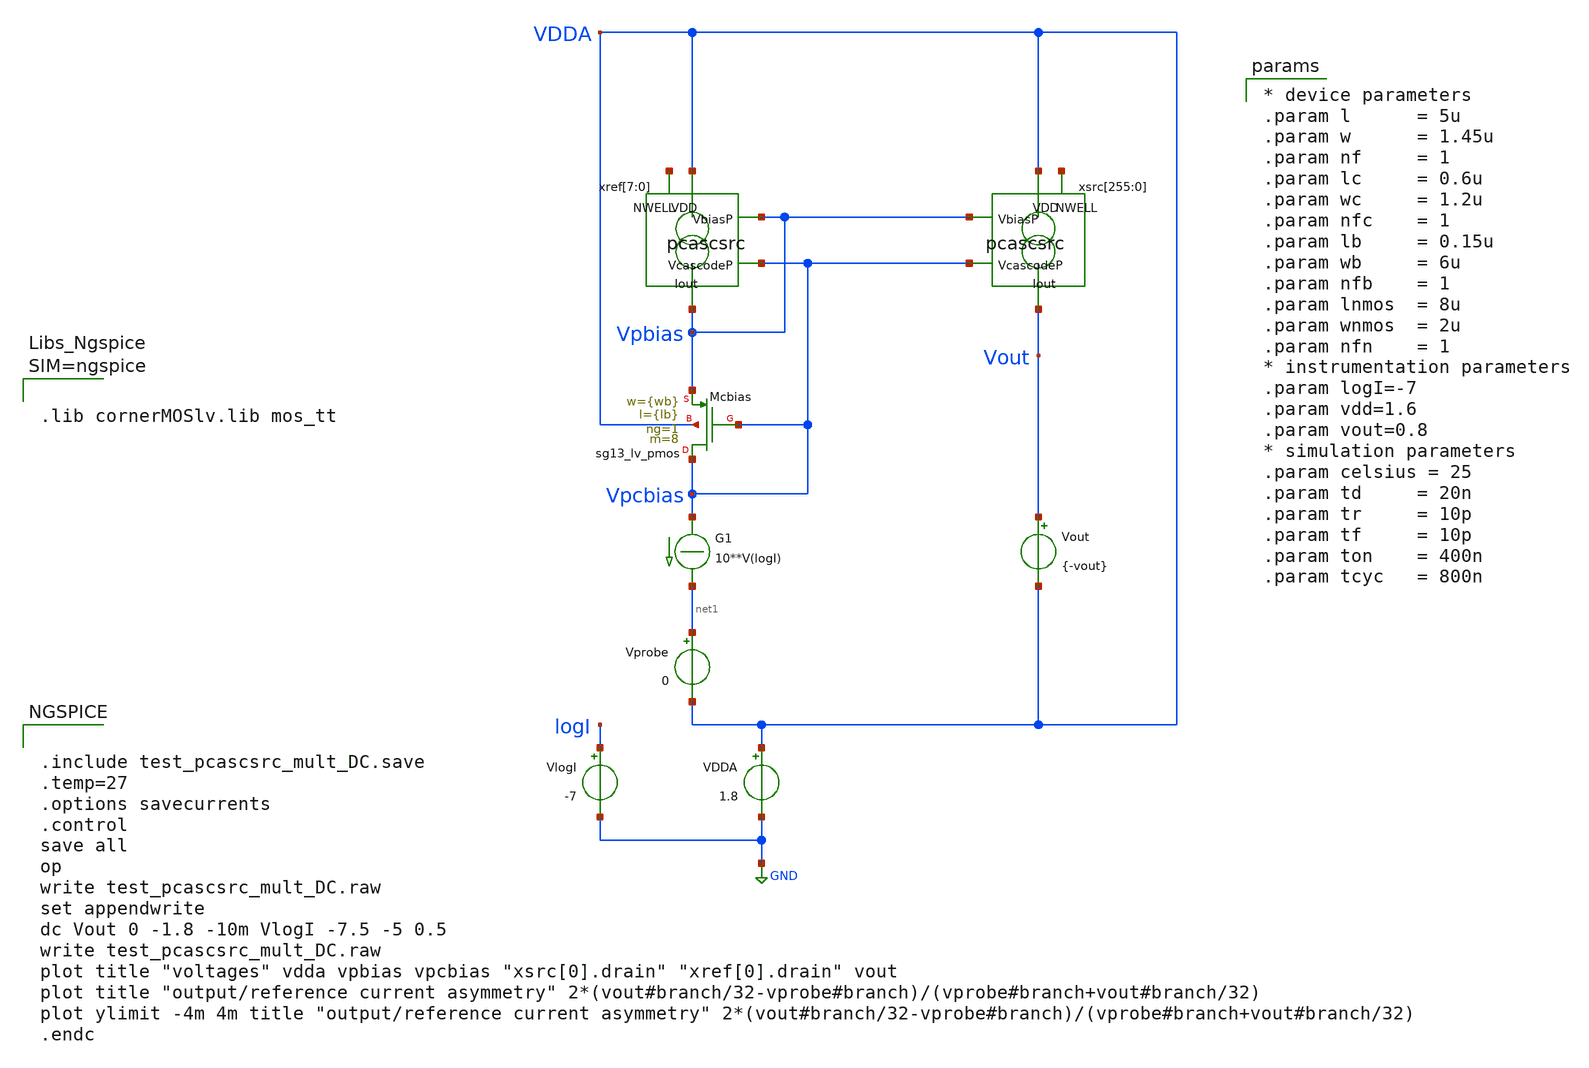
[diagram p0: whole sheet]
** sch_path: xschem/test_pcascsrc_mult_DC.sch
**.subckt test_pcascsrc_mult_DC
Vout Vout VDDA {-vout}
.save i(vout)
Vprobe net1 VDDA 0
.save i(vprobe)
G1 Vpcbias net1 CUR=' 10**V(logI) '
VlogI logI GND -7
.save i(vlogi)
xref[7] VDDA Vpbias Vpcbias Vpbias net2[7] pcascsrc
xref[6] VDDA Vpbias Vpcbias Vpbias net2[6] pcascsrc
xref[5] VDDA Vpbias Vpcbias Vpbias net2[5] pcascsrc
xref[4] VDDA Vpbias Vpcbias Vpbias net2[4] pcascsrc
xref[3] VDDA Vpbias Vpcbias Vpbias net2[3] pcascsrc
xref[2] VDDA Vpbias Vpcbias Vpbias net2[2] pcascsrc
xref[1] VDDA Vpbias Vpcbias Vpbias net2[1] pcascsrc
xref[0] VDDA Vpbias Vpcbias Vpbias net2[0] pcascsrc
xsrc[255] VDDA Vpbias Vpcbias Vout net3[255] pcascsrc
xsrc[254] VDDA Vpbias Vpcbias Vout net3[254] pcascsrc
xsrc[253] VDDA Vpbias Vpcbias Vout net3[253] pcascsrc
xsrc[252] VDDA Vpbias Vpcbias Vout net3[252] pcascsrc
xsrc[251] VDDA Vpbias Vpcbias Vout net3[251] pcascsrc
xsrc[250] VDDA Vpbias Vpcbias Vout net3[250] pcascsrc
xsrc[249] VDDA Vpbias Vpcbias Vout net3[249] pcascsrc
xsrc[248] VDDA Vpbias Vpcbias Vout net3[248] pcascsrc
xsrc[247] VDDA Vpbias Vpcbias Vout net3[247] pcascsrc
xsrc[246] VDDA Vpbias Vpcbias Vout net3[246] pcascsrc
xsrc[245] VDDA Vpbias Vpcbias Vout net3[245] pcascsrc
xsrc[244] VDDA Vpbias Vpcbias Vout net3[244] pcascsrc
xsrc[243] VDDA Vpbias Vpcbias Vout net3[243] pcascsrc
xsrc[242] VDDA Vpbias Vpcbias Vout net3[242] pcascsrc
xsrc[241] VDDA Vpbias Vpcbias Vout net3[241] pcascsrc
xsrc[240] VDDA Vpbias Vpcbias Vout net3[240] pcascsrc
xsrc[239] VDDA Vpbias Vpcbias Vout net3[239] pcascsrc
xsrc[238] VDDA Vpbias Vpcbias Vout net3[238] pcascsrc
xsrc[237] VDDA Vpbias Vpcbias Vout net3[237] pcascsrc
xsrc[236] VDDA Vpbias Vpcbias Vout net3[236] pcascsrc
xsrc[235] VDDA Vpbias Vpcbias Vout net3[235] pcascsrc
xsrc[234] VDDA Vpbias Vpcbias Vout net3[234] pcascsrc
xsrc[233] VDDA Vpbias Vpcbias Vout net3[233] pcascsrc
xsrc[232] VDDA Vpbias Vpcbias Vout net3[232] pcascsrc
xsrc[231] VDDA Vpbias Vpcbias Vout net3[231] pcascsrc
xsrc[230] VDDA Vpbias Vpcbias Vout net3[230] pcascsrc
xsrc[229] VDDA Vpbias Vpcbias Vout net3[229] pcascsrc
xsrc[228] VDDA Vpbias Vpcbias Vout net3[228] pcascsrc
xsrc[227] VDDA Vpbias Vpcbias Vout net3[227] pcascsrc
xsrc[226] VDDA Vpbias Vpcbias Vout net3[226] pcascsrc
xsrc[225] VDDA Vpbias Vpcbias Vout net3[225] pcascsrc
xsrc[224] VDDA Vpbias Vpcbias Vout net3[224] pcascsrc
xsrc[223] VDDA Vpbias Vpcbias Vout net3[223] pcascsrc
xsrc[222] VDDA Vpbias Vpcbias Vout net3[222] pcascsrc
xsrc[221] VDDA Vpbias Vpcbias Vout net3[221] pcascsrc
xsrc[220] VDDA Vpbias Vpcbias Vout net3[220] pcascsrc
xsrc[219] VDDA Vpbias Vpcbias Vout net3[219] pcascsrc
xsrc[218] VDDA Vpbias Vpcbias Vout net3[218] pcascsrc
xsrc[217] VDDA Vpbias Vpcbias Vout net3[217] pcascsrc
xsrc[216] VDDA Vpbias Vpcbias Vout net3[216] pcascsrc
xsrc[215] VDDA Vpbias Vpcbias Vout net3[215] pcascsrc
xsrc[214] VDDA Vpbias Vpcbias Vout net3[214] pcascsrc
xsrc[213] VDDA Vpbias Vpcbias Vout net3[213] pcascsrc
xsrc[212] VDDA Vpbias Vpcbias Vout net3[212] pcascsrc
xsrc[211] VDDA Vpbias Vpcbias Vout net3[211] pcascsrc
xsrc[210] VDDA Vpbias Vpcbias Vout net3[210] pcascsrc
xsrc[209] VDDA Vpbias Vpcbias Vout net3[209] pcascsrc
xsrc[208] VDDA Vpbias Vpcbias Vout net3[208] pcascsrc
xsrc[207] VDDA Vpbias Vpcbias Vout net3[207] pcascsrc
xsrc[206] VDDA Vpbias Vpcbias Vout net3[206] pcascsrc
xsrc[205] VDDA Vpbias Vpcbias Vout net3[205] pcascsrc
xsrc[204] VDDA Vpbias Vpcbias Vout net3[204] pcascsrc
xsrc[203] VDDA Vpbias Vpcbias Vout net3[203] pcascsrc
xsrc[202] VDDA Vpbias Vpcbias Vout net3[202] pcascsrc
xsrc[201] VDDA Vpbias Vpcbias Vout net3[201] pcascsrc
xsrc[200] VDDA Vpbias Vpcbias Vout net3[200] pcascsrc
xsrc[199] VDDA Vpbias Vpcbias Vout net3[199] pcascsrc
xsrc[198] VDDA Vpbias Vpcbias Vout net3[198] pcascsrc
xsrc[197] VDDA Vpbias Vpcbias Vout net3[197] pcascsrc
xsrc[196] VDDA Vpbias Vpcbias Vout net3[196] pcascsrc
xsrc[195] VDDA Vpbias Vpcbias Vout net3[195] pcascsrc
xsrc[194] VDDA Vpbias Vpcbias Vout net3[194] pcascsrc
xsrc[193] VDDA Vpbias Vpcbias Vout net3[193] pcascsrc
xsrc[192] VDDA Vpbias Vpcbias Vout net3[192] pcascsrc
xsrc[191] VDDA Vpbias Vpcbias Vout net3[191] pcascsrc
xsrc[190] VDDA Vpbias Vpcbias Vout net3[190] pcascsrc
xsrc[189] VDDA Vpbias Vpcbias Vout net3[189] pcascsrc
xsrc[188] VDDA Vpbias Vpcbias Vout net3[188] pcascsrc
xsrc[187] VDDA Vpbias Vpcbias Vout net3[187] pcascsrc
xsrc[186] VDDA Vpbias Vpcbias Vout net3[186] pcascsrc
xsrc[185] VDDA Vpbias Vpcbias Vout net3[185] pcascsrc
xsrc[184] VDDA Vpbias Vpcbias Vout net3[184] pcascsrc
xsrc[183] VDDA Vpbias Vpcbias Vout net3[183] pcascsrc
xsrc[182] VDDA Vpbias Vpcbias Vout net3[182] pcascsrc
xsrc[181] VDDA Vpbias Vpcbias Vout net3[181] pcascsrc
xsrc[180] VDDA Vpbias Vpcbias Vout net3[180] pcascsrc
xsrc[179] VDDA Vpbias Vpcbias Vout net3[179] pcascsrc
xsrc[178] VDDA Vpbias Vpcbias Vout net3[178] pcascsrc
xsrc[177] VDDA Vpbias Vpcbias Vout net3[177] pcascsrc
xsrc[176] VDDA Vpbias Vpcbias Vout net3[176] pcascsrc
xsrc[175] VDDA Vpbias Vpcbias Vout net3[175] pcascsrc
xsrc[174] VDDA Vpbias Vpcbias Vout net3[174] pcascsrc
xsrc[173] VDDA Vpbias Vpcbias Vout net3[173] pcascsrc
xsrc[172] VDDA Vpbias Vpcbias Vout net3[172] pcascsrc
xsrc[171] VDDA Vpbias Vpcbias Vout net3[171] pcascsrc
xsrc[170] VDDA Vpbias Vpcbias Vout net3[170] pcascsrc
xsrc[169] VDDA Vpbias Vpcbias Vout net3[169] pcascsrc
xsrc[168] VDDA Vpbias Vpcbias Vout net3[168] pcascsrc
xsrc[167] VDDA Vpbias Vpcbias Vout net3[167] pcascsrc
xsrc[166] VDDA Vpbias Vpcbias Vout net3[166] pcascsrc
xsrc[165] VDDA Vpbias Vpcbias Vout net3[165] pcascsrc
xsrc[164] VDDA Vpbias Vpcbias Vout net3[164] pcascsrc
xsrc[163] VDDA Vpbias Vpcbias Vout net3[163] pcascsrc
xsrc[162] VDDA Vpbias Vpcbias Vout net3[162] pcascsrc
xsrc[161] VDDA Vpbias Vpcbias Vout net3[161] pcascsrc
xsrc[160] VDDA Vpbias Vpcbias Vout net3[160] pcascsrc
xsrc[159] VDDA Vpbias Vpcbias Vout net3[159] pcascsrc
xsrc[158] VDDA Vpbias Vpcbias Vout net3[158] pcascsrc
xsrc[157] VDDA Vpbias Vpcbias Vout net3[157] pcascsrc
xsrc[156] VDDA Vpbias Vpcbias Vout net3[156] pcascsrc
xsrc[155] VDDA Vpbias Vpcbias Vout net3[155] pcascsrc
xsrc[154] VDDA Vpbias Vpcbias Vout net3[154] pcascsrc
xsrc[153] VDDA Vpbias Vpcbias Vout net3[153] pcascsrc
xsrc[152] VDDA Vpbias Vpcbias Vout net3[152] pcascsrc
xsrc[151] VDDA Vpbias Vpcbias Vout net3[151] pcascsrc
xsrc[150] VDDA Vpbias Vpcbias Vout net3[150] pcascsrc
xsrc[149] VDDA Vpbias Vpcbias Vout net3[149] pcascsrc
xsrc[148] VDDA Vpbias Vpcbias Vout net3[148] pcascsrc
xsrc[147] VDDA Vpbias Vpcbias Vout net3[147] pcascsrc
xsrc[146] VDDA Vpbias Vpcbias Vout net3[146] pcascsrc
xsrc[145] VDDA Vpbias Vpcbias Vout net3[145] pcascsrc
xsrc[144] VDDA Vpbias Vpcbias Vout net3[144] pcascsrc
xsrc[143] VDDA Vpbias Vpcbias Vout net3[143] pcascsrc
xsrc[142] VDDA Vpbias Vpcbias Vout net3[142] pcascsrc
xsrc[141] VDDA Vpbias Vpcbias Vout net3[141] pcascsrc
xsrc[140] VDDA Vpbias Vpcbias Vout net3[140] pcascsrc
xsrc[139] VDDA Vpbias Vpcbias Vout net3[139] pcascsrc
xsrc[138] VDDA Vpbias Vpcbias Vout net3[138] pcascsrc
xsrc[137] VDDA Vpbias Vpcbias Vout net3[137] pcascsrc
xsrc[136] VDDA Vpbias Vpcbias Vout net3[136] pcascsrc
xsrc[135] VDDA Vpbias Vpcbias Vout net3[135] pcascsrc
xsrc[134] VDDA Vpbias Vpcbias Vout net3[134] pcascsrc
xsrc[133] VDDA Vpbias Vpcbias Vout net3[133] pcascsrc
xsrc[132] VDDA Vpbias Vpcbias Vout net3[132] pcascsrc
xsrc[131] VDDA Vpbias Vpcbias Vout net3[131] pcascsrc
xsrc[130] VDDA Vpbias Vpcbias Vout net3[130] pcascsrc
xsrc[129] VDDA Vpbias Vpcbias Vout net3[129] pcascsrc
xsrc[128] VDDA Vpbias Vpcbias Vout net3[128] pcascsrc
xsrc[127] VDDA Vpbias Vpcbias Vout net3[127] pcascsrc
xsrc[126] VDDA Vpbias Vpcbias Vout net3[126] pcascsrc
xsrc[125] VDDA Vpbias Vpcbias Vout net3[125] pcascsrc
xsrc[124] VDDA Vpbias Vpcbias Vout net3[124] pcascsrc
xsrc[123] VDDA Vpbias Vpcbias Vout net3[123] pcascsrc
xsrc[122] VDDA Vpbias Vpcbias Vout net3[122] pcascsrc
xsrc[121] VDDA Vpbias Vpcbias Vout net3[121] pcascsrc
xsrc[120] VDDA Vpbias Vpcbias Vout net3[120] pcascsrc
xsrc[119] VDDA Vpbias Vpcbias Vout net3[119] pcascsrc
xsrc[118] VDDA Vpbias Vpcbias Vout net3[118] pcascsrc
xsrc[117] VDDA Vpbias Vpcbias Vout net3[117] pcascsrc
xsrc[116] VDDA Vpbias Vpcbias Vout net3[116] pcascsrc
xsrc[115] VDDA Vpbias Vpcbias Vout net3[115] pcascsrc
xsrc[114] VDDA Vpbias Vpcbias Vout net3[114] pcascsrc
xsrc[113] VDDA Vpbias Vpcbias Vout net3[113] pcascsrc
xsrc[112] VDDA Vpbias Vpcbias Vout net3[112] pcascsrc
xsrc[111] VDDA Vpbias Vpcbias Vout net3[111] pcascsrc
xsrc[110] VDDA Vpbias Vpcbias Vout net3[110] pcascsrc
xsrc[109] VDDA Vpbias Vpcbias Vout net3[109] pcascsrc
xsrc[108] VDDA Vpbias Vpcbias Vout net3[108] pcascsrc
xsrc[107] VDDA Vpbias Vpcbias Vout net3[107] pcascsrc
xsrc[106] VDDA Vpbias Vpcbias Vout net3[106] pcascsrc
xsrc[105] VDDA Vpbias Vpcbias Vout net3[105] pcascsrc
xsrc[104] VDDA Vpbias Vpcbias Vout net3[104] pcascsrc
xsrc[103] VDDA Vpbias Vpcbias Vout net3[103] pcascsrc
xsrc[102] VDDA Vpbias Vpcbias Vout net3[102] pcascsrc
xsrc[101] VDDA Vpbias Vpcbias Vout net3[101] pcascsrc
xsrc[100] VDDA Vpbias Vpcbias Vout net3[100] pcascsrc
xsrc[99] VDDA Vpbias Vpcbias Vout net3[99] pcascsrc
xsrc[98] VDDA Vpbias Vpcbias Vout net3[98] pcascsrc
xsrc[97] VDDA Vpbias Vpcbias Vout net3[97] pcascsrc
xsrc[96] VDDA Vpbias Vpcbias Vout net3[96] pcascsrc
xsrc[95] VDDA Vpbias Vpcbias Vout net3[95] pcascsrc
xsrc[94] VDDA Vpbias Vpcbias Vout net3[94] pcascsrc
xsrc[93] VDDA Vpbias Vpcbias Vout net3[93] pcascsrc
xsrc[92] VDDA Vpbias Vpcbias Vout net3[92] pcascsrc
xsrc[91] VDDA Vpbias Vpcbias Vout net3[91] pcascsrc
xsrc[90] VDDA Vpbias Vpcbias Vout net3[90] pcascsrc
xsrc[89] VDDA Vpbias Vpcbias Vout net3[89] pcascsrc
xsrc[88] VDDA Vpbias Vpcbias Vout net3[88] pcascsrc
xsrc[87] VDDA Vpbias Vpcbias Vout net3[87] pcascsrc
xsrc[86] VDDA Vpbias Vpcbias Vout net3[86] pcascsrc
xsrc[85] VDDA Vpbias Vpcbias Vout net3[85] pcascsrc
xsrc[84] VDDA Vpbias Vpcbias Vout net3[84] pcascsrc
xsrc[83] VDDA Vpbias Vpcbias Vout net3[83] pcascsrc
xsrc[82] VDDA Vpbias Vpcbias Vout net3[82] pcascsrc
xsrc[81] VDDA Vpbias Vpcbias Vout net3[81] pcascsrc
xsrc[80] VDDA Vpbias Vpcbias Vout net3[80] pcascsrc
xsrc[79] VDDA Vpbias Vpcbias Vout net3[79] pcascsrc
xsrc[78] VDDA Vpbias Vpcbias Vout net3[78] pcascsrc
xsrc[77] VDDA Vpbias Vpcbias Vout net3[77] pcascsrc
xsrc[76] VDDA Vpbias Vpcbias Vout net3[76] pcascsrc
xsrc[75] VDDA Vpbias Vpcbias Vout net3[75] pcascsrc
xsrc[74] VDDA Vpbias Vpcbias Vout net3[74] pcascsrc
xsrc[73] VDDA Vpbias Vpcbias Vout net3[73] pcascsrc
xsrc[72] VDDA Vpbias Vpcbias Vout net3[72] pcascsrc
xsrc[71] VDDA Vpbias Vpcbias Vout net3[71] pcascsrc
xsrc[70] VDDA Vpbias Vpcbias Vout net3[70] pcascsrc
xsrc[69] VDDA Vpbias Vpcbias Vout net3[69] pcascsrc
xsrc[68] VDDA Vpbias Vpcbias Vout net3[68] pcascsrc
xsrc[67] VDDA Vpbias Vpcbias Vout net3[67] pcascsrc
xsrc[66] VDDA Vpbias Vpcbias Vout net3[66] pcascsrc
xsrc[65] VDDA Vpbias Vpcbias Vout net3[65] pcascsrc
xsrc[64] VDDA Vpbias Vpcbias Vout net3[64] pcascsrc
xsrc[63] VDDA Vpbias Vpcbias Vout net3[63] pcascsrc
xsrc[62] VDDA Vpbias Vpcbias Vout net3[62] pcascsrc
xsrc[61] VDDA Vpbias Vpcbias Vout net3[61] pcascsrc
xsrc[60] VDDA Vpbias Vpcbias Vout net3[60] pcascsrc
xsrc[59] VDDA Vpbias Vpcbias Vout net3[59] pcascsrc
xsrc[58] VDDA Vpbias Vpcbias Vout net3[58] pcascsrc
xsrc[57] VDDA Vpbias Vpcbias Vout net3[57] pcascsrc
xsrc[56] VDDA Vpbias Vpcbias Vout net3[56] pcascsrc
xsrc[55] VDDA Vpbias Vpcbias Vout net3[55] pcascsrc
xsrc[54] VDDA Vpbias Vpcbias Vout net3[54] pcascsrc
xsrc[53] VDDA Vpbias Vpcbias Vout net3[53] pcascsrc
xsrc[52] VDDA Vpbias Vpcbias Vout net3[52] pcascsrc
xsrc[51] VDDA Vpbias Vpcbias Vout net3[51] pcascsrc
xsrc[50] VDDA Vpbias Vpcbias Vout net3[50] pcascsrc
xsrc[49] VDDA Vpbias Vpcbias Vout net3[49] pcascsrc
xsrc[48] VDDA Vpbias Vpcbias Vout net3[48] pcascsrc
xsrc[47] VDDA Vpbias Vpcbias Vout net3[47] pcascsrc
xsrc[46] VDDA Vpbias Vpcbias Vout net3[46] pcascsrc
xsrc[45] VDDA Vpbias Vpcbias Vout net3[45] pcascsrc
xsrc[44] VDDA Vpbias Vpcbias Vout net3[44] pcascsrc
xsrc[43] VDDA Vpbias Vpcbias Vout net3[43] pcascsrc
xsrc[42] VDDA Vpbias Vpcbias Vout net3[42] pcascsrc
xsrc[41] VDDA Vpbias Vpcbias Vout net3[41] pcascsrc
xsrc[40] VDDA Vpbias Vpcbias Vout net3[40] pcascsrc
xsrc[39] VDDA Vpbias Vpcbias Vout net3[39] pcascsrc
xsrc[38] VDDA Vpbias Vpcbias Vout net3[38] pcascsrc
xsrc[37] VDDA Vpbias Vpcbias Vout net3[37] pcascsrc
xsrc[36] VDDA Vpbias Vpcbias Vout net3[36] pcascsrc
xsrc[35] VDDA Vpbias Vpcbias Vout net3[35] pcascsrc
xsrc[34] VDDA Vpbias Vpcbias Vout net3[34] pcascsrc
xsrc[33] VDDA Vpbias Vpcbias Vout net3[33] pcascsrc
xsrc[32] VDDA Vpbias Vpcbias Vout net3[32] pcascsrc
xsrc[31] VDDA Vpbias Vpcbias Vout net3[31] pcascsrc
xsrc[30] VDDA Vpbias Vpcbias Vout net3[30] pcascsrc
xsrc[29] VDDA Vpbias Vpcbias Vout net3[29] pcascsrc
xsrc[28] VDDA Vpbias Vpcbias Vout net3[28] pcascsrc
xsrc[27] VDDA Vpbias Vpcbias Vout net3[27] pcascsrc
xsrc[26] VDDA Vpbias Vpcbias Vout net3[26] pcascsrc
xsrc[25] VDDA Vpbias Vpcbias Vout net3[25] pcascsrc
xsrc[24] VDDA Vpbias Vpcbias Vout net3[24] pcascsrc
xsrc[23] VDDA Vpbias Vpcbias Vout net3[23] pcascsrc
xsrc[22] VDDA Vpbias Vpcbias Vout net3[22] pcascsrc
xsrc[21] VDDA Vpbias Vpcbias Vout net3[21] pcascsrc
xsrc[20] VDDA Vpbias Vpcbias Vout net3[20] pcascsrc
xsrc[19] VDDA Vpbias Vpcbias Vout net3[19] pcascsrc
xsrc[18] VDDA Vpbias Vpcbias Vout net3[18] pcascsrc
xsrc[17] VDDA Vpbias Vpcbias Vout net3[17] pcascsrc
xsrc[16] VDDA Vpbias Vpcbias Vout net3[16] pcascsrc
xsrc[15] VDDA Vpbias Vpcbias Vout net3[15] pcascsrc
xsrc[14] VDDA Vpbias Vpcbias Vout net3[14] pcascsrc
xsrc[13] VDDA Vpbias Vpcbias Vout net3[13] pcascsrc
xsrc[12] VDDA Vpbias Vpcbias Vout net3[12] pcascsrc
xsrc[11] VDDA Vpbias Vpcbias Vout net3[11] pcascsrc
xsrc[10] VDDA Vpbias Vpcbias Vout net3[10] pcascsrc
xsrc[9] VDDA Vpbias Vpcbias Vout net3[9] pcascsrc
xsrc[8] VDDA Vpbias Vpcbias Vout net3[8] pcascsrc
xsrc[7] VDDA Vpbias Vpcbias Vout net3[7] pcascsrc
xsrc[6] VDDA Vpbias Vpcbias Vout net3[6] pcascsrc
xsrc[5] VDDA Vpbias Vpcbias Vout net3[5] pcascsrc
xsrc[4] VDDA Vpbias Vpcbias Vout net3[4] pcascsrc
xsrc[3] VDDA Vpbias Vpcbias Vout net3[3] pcascsrc
xsrc[2] VDDA Vpbias Vpcbias Vout net3[2] pcascsrc
xsrc[1] VDDA Vpbias Vpcbias Vout net3[1] pcascsrc
xsrc[0] VDDA Vpbias Vpcbias Vout net3[0] pcascsrc
VDDA VDDA GND 1.8
.save i(vdda)
XMcbias Vpcbias Vpcbias Vpbias VDDA sg13_lv_pmos w={wb} l={lb} ng=1 m=8 mm_ok=1
**** begin user architecture code


.include test_pcascsrc_mult_DC.save
.temp=27
.options savecurrents
.control
save all
op
write test_pcascsrc_mult_DC.raw
set appendwrite
dc Vout 0 -1.8 -10m VlogI -7.5 -5 0.5
write test_pcascsrc_mult_DC.raw
plot title "voltages" vdda vpbias vpcbias "xsrc[0].drain" "xref[0].drain" vout
plot title "output/reference current asymmetry"
+ 2*(vout#branch/32-vprobe#branch)/(vprobe#branch+vout#branch/32)
plot ylimit -4m 4m title "output/reference current asymmetry"
+ 2*(vout#branch/32-vprobe#branch)/(vprobe#branch+vout#branch/32)
.endc





.lib cornerMOSlv.lib mos_tt




* device parameters
.param l      = 5u
.param w      = 1.45u
.param nf     = 1
.param lc     = 0.6u
.param wc     = 1.2u
.param nfc    = 1
.param lb     = 0.15u
.param wb     = 6u
.param nfb    = 1
.param lnmos  = 8u
.param wnmos  = 2u
.param nfn    = 1
* instrumentation parameters
.param logI=-7
.param vdd=1.6
.param vout=0.8
* simulation parameters
.param celsius = 25
.param td     = 20n
.param tr     = 10p
.param tf     = 10p
.param ton    = 400n
.param tcyc   = 800n


**** end user architecture code
**.ends

* expanding   symbol:  pcascsrc.sym # of pins=5
** sym_path: xschem/pcascsrc.sym
** sch_path: xschem/pcascsrc.sch
.subckt pcascsrc VDD VbiasP VcascodeP Iout NWELL
*.ipin VcascodeP
*.ipin VbiasP
*.opin Iout
*.ipin VDD
*.iopin NWELL
XMsrc drain VbiasP VDD NWELL sg13_lv_pmos w=0.74u l=2u ng=1 m=1 mm_ok=1
XMcasc Iout VcascodeP drain NWELL sg13_lv_pmos w=0.3u l=0.3u ng=1 m=1 mm_ok=1
.ends

.GLOBAL GND
.end
